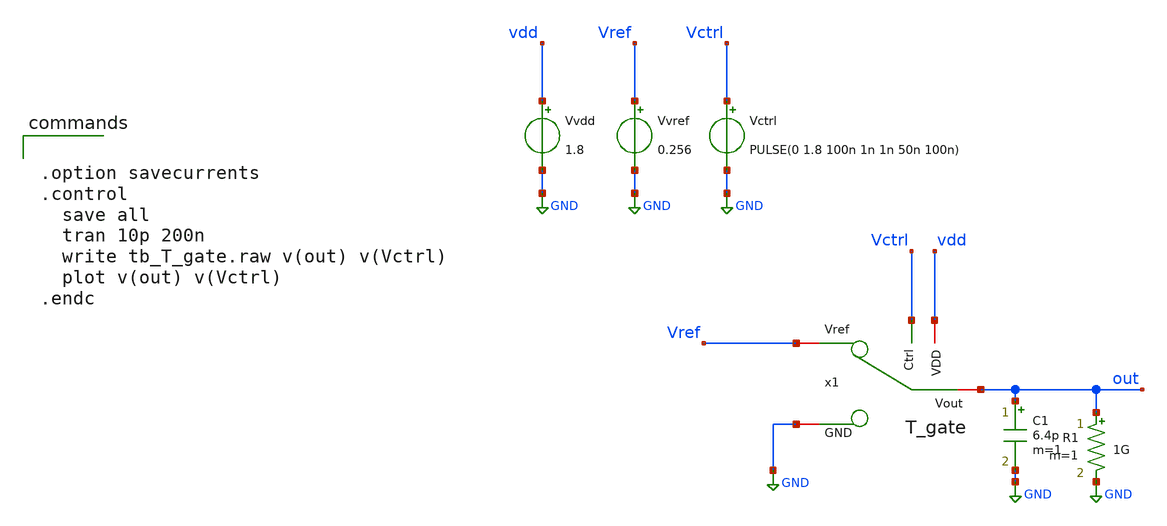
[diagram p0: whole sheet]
** sch_path: 05_mixed_signal/soluzioni/lab01/xschem/tb_T_gate.sch
**.subckt tb_T_gate
x1 vdd GND Vctrl out Vref T_gate
Vvdd vdd GND 1.8
Vvref Vref GND 0.256
Vctrl Vctrl GND PULSE(0 1.8 100n 1n 1n 50n 100n)
C1 out GND 6.4p m=1
R1 out GND 1G m=1
**** begin user architecture code

** opencircuitdesign pdks install
.lib $::SKYWATER_MODELS/sky130.lib.spice tt



.option savecurrents
.control
  save all
  tran 10p 200n
  write tb_T_gate.raw v(out) v(Vctrl)
  plot v(out) v(Vctrl)
.endc


**** end user architecture code
**.ends

* expanding   symbol:  T_gate.sym # of pins=5
** sym_path: 05_mixed_signal/soluzioni/lab01/xschem/T_gate.sym
** sch_path: 05_mixed_signal/soluzioni/lab01/xschem/T_gate.sch
.subckt T_gate VDD GND Ctrl Vout Vref
*.ipin Ctrl
*.iopin Vout
*.iopin VDD
*.iopin GND
*.iopin Vref
x1 VDD Ctrl net1 GND inverter
XM1 GND net1 Vout GND sky130_fd_pr__nfet_01v8_lvt L=0.15 W=2 nf=1 ad='int((1 + 1)/2) * 2 / 1 * 0.29'
+ as='int((1 + 2)/2) * 2 / 1 * 0.29' pd='2*int((1 + 1)/2) * (2 / 1 + 0.29)' ps='2*int((1 + 2)/2) * (2 / 1 + 0.29)'
+ nrd='0.29 / 2 ' nrs='0.29 / 2 ' sa=0 sb=0 sd=0 mult=1 m=1
XM2 GND Ctrl Vout VDD sky130_fd_pr__pfet_01v8_lvt L=0.35 W=4 nf=1 ad='int((1 + 1)/2) * 4 / 1 * 0.29'
+ as='int((1 + 2)/2) * 4 / 1 * 0.29' pd='2*int((1 + 1)/2) * (4 / 1 + 0.29)' ps='2*int((1 + 2)/2) * (4 / 1 + 0.29)'
+ nrd='0.29 / 4 ' nrs='0.29 / 4 ' sa=0 sb=0 sd=0 mult=1 m=1
XM3 Vref Ctrl Vout GND sky130_fd_pr__nfet_01v8_lvt L=0.15 W=2 nf=1 ad='int((1 + 1)/2) * 2 / 1 * 0.29'
+ as='int((1 + 2)/2) * 2 / 1 * 0.29' pd='2*int((1 + 1)/2) * (2 / 1 + 0.29)' ps='2*int((1 + 2)/2) * (2 / 1 + 0.29)'
+ nrd='0.29 / 2 ' nrs='0.29 / 2 ' sa=0 sb=0 sd=0 mult=1 m=1
XM4 Vref net1 Vout VDD sky130_fd_pr__pfet_01v8_lvt L=0.35 W=4 nf=1 ad='int((1 + 1)/2) * 4 / 1 * 0.29'
+ as='int((1 + 2)/2) * 4 / 1 * 0.29' pd='2*int((1 + 1)/2) * (4 / 1 + 0.29)' ps='2*int((1 + 2)/2) * (4 / 1 + 0.29)'
+ nrd='0.29 / 4 ' nrs='0.29 / 4 ' sa=0 sb=0 sd=0 mult=1 m=1
.ends


* expanding   symbol:  inverter.sym # of pins=4
** sym_path: 05_mixed_signal/soluzioni/lab03/xschem/inverter.sym
** sch_path: 05_mixed_signal/soluzioni/lab03/xschem/inverter.sch
.subckt inverter VDD IN OUT GND
*.ipin IN
*.opin OUT
*.iopin VDD
*.iopin GND
XM1 OUT IN GND GND sky130_fd_pr__nfet_01v8_lvt L=0.15 W=2 nf=1 ad='int((1 + 1)/2) * 2 / 1 * 0.29' as='int((1 + 2)/2) * 2 / 1 * 0.29'
+ pd='2*int((1 + 1)/2) * (2 / 1 + 0.29)' ps='2*int((1 + 2)/2) * (2 / 1 + 0.29)' nrd='0.29 / 2 ' nrs='0.29 / 2 '
+ sa=0 sb=0 sd=0 mult=1 m=1
XM2 OUT IN VDD VDD sky130_fd_pr__pfet_01v8_lvt L=0.35 W=4 nf=1 ad='int((1 + 1)/2) * 4 / 1 * 0.29' as='int((1 + 2)/2) * 4 / 1 * 0.29'
+ pd='2*int((1 + 1)/2) * (4 / 1 + 0.29)' ps='2*int((1 + 2)/2) * (4 / 1 + 0.29)' nrd='0.29 / 4 ' nrs='0.29 / 4 '
+ sa=0 sb=0 sd=0 mult=1 m=1
.ends

.GLOBAL GND
.end
